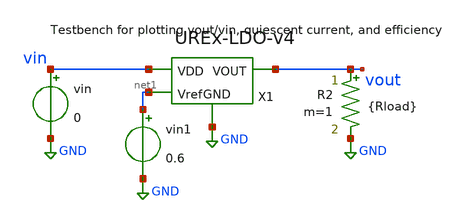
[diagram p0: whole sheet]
** sch_path: xschem/testbenches/VoutvsVin-v4.sch
**.subckt VoutvsVin-v4
vin vin GND 0
R2 vout GND {Rload} m=1
X1 vin vout GND net1 UREx-LDO-v4
vin1 net1 GND 0.6
**** begin user architecture code



.lib /usr/local/share/pdk/sky130A/libs.tech/ngspice/sky130.lib.spice tt
.param Rload = 20
.dc vin 0.5 5 0.1
*.tran 5u 10m

.control
run
let Rload = 20
let iout = vout/Rload
let iq = (-i(vin))-iout
let eff = (iout*vout*100)/((iout+iq)*vin)

plot v(vout)
plot iq
plot eff

.endc


**** end user architecture code
**.ends

* expanding   symbol:  UREx-LDO-v4.sym # of pins=4
** sym_path: xschem/UREx-LDO-v4.sym
** sch_path: xschem/UREx-LDO-v4.sch
.subckt UREx-LDO-v4 VDD VOUT GND Vref
*.ipin VDD
*.opin VOUT
*.ipin GND
*.ipin Vref
XM1 net3 Vref net1 GND sky130_fd_pr__nfet_01v8_lvt L=1 W=0.8 nf=1 ad='int((1 + 1)/2) * 0.8 / 1 * 0.29'
+ as='int((1 + 2)/2) * 0.8 / 1 * 0.29' pd='2*int((1 + 1)/2) * (0.8 / 1 + 0.29)' ps='2*int((1 + 2)/2) * (0.8 / 1 + 0.29)'
+ nrd='0.29 / 0.8 ' nrs='0.29 / 0.8 ' sa=0 sb=0 sd=0 mult=1 m=1
XM2 net2 v+ net1 GND sky130_fd_pr__nfet_01v8_lvt L=1 W=0.8 nf=1 ad='int((1 + 1)/2) * 0.8 / 1 * 0.29'
+ as='int((1 + 2)/2) * 0.8 / 1 * 0.29' pd='2*int((1 + 1)/2) * (0.8 / 1 + 0.29)' ps='2*int((1 + 2)/2) * (0.8 / 1 + 0.29)'
+ nrd='0.29 / 0.8 ' nrs='0.29 / 0.8 ' sa=0 sb=0 sd=0 mult=1 m=1
XM4 net2 net3 VDD VDD sky130_fd_pr__pfet_01v8_lvt L=1 W=0.5 nf=1 ad='int((1 + 1)/2) * 0.5 / 1 * 0.29'
+ as='int((1 + 2)/2) * 0.5 / 1 * 0.29' pd='2*int((1 + 1)/2) * (0.5 / 1 + 0.29)' ps='2*int((1 + 2)/2) * (0.5 / 1 + 0.29)'
+ nrd='0.29 / 0.5 ' nrs='0.29 / 0.5 ' sa=0 sb=0 sd=0 mult=1 m=1
XM3 net3 net3 VDD VDD sky130_fd_pr__pfet_01v8_lvt L=1 W=0.5 nf=1 ad='int((1 + 1)/2) * 0.5 / 1 * 0.29'
+ as='int((1 + 2)/2) * 0.5 / 1 * 0.29' pd='2*int((1 + 1)/2) * (0.5 / 1 + 0.29)' ps='2*int((1 + 2)/2) * (0.5 / 1 + 0.29)'
+ nrd='0.29 / 0.5 ' nrs='0.29 / 0.5 ' sa=0 sb=0 sd=0 mult=1 m=1
XM6 gate net2 VDD VDD sky130_fd_pr__pfet_01v8_lvt L=0.35 W=4.2 nf=1 ad='int((1 + 1)/2) * 4.2 / 1 * 0.29'
+ as='int((1 + 2)/2) * 4.2 / 1 * 0.29' pd='2*int((1 + 1)/2) * (4.2 / 1 + 0.29)' ps='2*int((1 + 2)/2) * (4.2 / 1 + 0.29)'
+ nrd='0.29 / 4.2 ' nrs='0.29 / 4.2 ' sa=0 sb=0 sd=0 mult=1 m=1
XM7 gate net4 GND GND sky130_fd_pr__nfet_01v8_lvt L=0.25 W=5.2 nf=1 ad='int((1 + 1)/2) * 5.2 / 1 * 0.29'
+ as='int((1 + 2)/2) * 5.2 / 1 * 0.29' pd='2*int((1 + 1)/2) * (5.2 / 1 + 0.29)' ps='2*int((1 + 2)/2) * (5.2 / 1 + 0.29)'
+ nrd='0.29 / 5.2 ' nrs='0.29 / 5.2 ' sa=0 sb=0 sd=0 mult=1 m=1
XM9 VOUT gate VDD VDD sky130_fd_pr__pfet_01v8_lvt L=0.35 W=1750 nf=50 ad='int((50 + 1)/2) * 1750 / 50 * 0.29'
+ as='int((50 + 2)/2) * 1750 / 50 * 0.29' pd='2*int((50 + 1)/2) * (1750 / 50 + 0.29)' ps='2*int((50 + 2)/2) * (1750 / 50 + 0.29)'
+ nrd='0.29 / 1750 ' nrs='0.29 / 1750 ' sa=0 sb=0 sd=0 mult=1 m=1
XM10 net4 net5 VDD VDD sky130_fd_pr__pfet_01v8_lvt L=1 W=1 nf=1 ad='int((1 + 1)/2) * 1 / 1 * 0.29' as='int((1 + 2)/2) * 1 / 1 * 0.29'
+ pd='2*int((1 + 1)/2) * (1 / 1 + 0.29)' ps='2*int((1 + 2)/2) * (1 / 1 + 0.29)' nrd='0.29 / 1 ' nrs='0.29 / 1 '
+ sa=0 sb=0 sd=0 mult=1 m=1
XM11 net5 net5 VDD VDD sky130_fd_pr__pfet_01v8_lvt L=1 W=1 nf=1 ad='int((1 + 1)/2) * 1 / 1 * 0.29' as='int((1 + 2)/2) * 1 / 1 * 0.29'
+ pd='2*int((1 + 1)/2) * (1 / 1 + 0.29)' ps='2*int((1 + 2)/2) * (1 / 1 + 0.29)' nrd='0.29 / 1 ' nrs='0.29 / 1 '
+ sa=0 sb=0 sd=0 mult=1 m=1
XM12 net7 net5 VDD VDD sky130_fd_pr__pfet_01v8_lvt L=1 W=1 nf=1 ad='int((1 + 1)/2) * 1 / 1 * 0.29' as='int((1 + 2)/2) * 1 / 1 * 0.29'
+ pd='2*int((1 + 1)/2) * (1 / 1 + 0.29)' ps='2*int((1 + 2)/2) * (1 / 1 + 0.29)' nrd='0.29 / 1 ' nrs='0.29 / 1 '
+ sa=0 sb=0 sd=0 mult=1 m=1
XM13 net7 net7 GND GND sky130_fd_pr__nfet_01v8_lvt L=1 W=2 nf=1 ad='int((1 + 1)/2) * 2 / 1 * 0.29' as='int((1 + 2)/2) * 2 / 1 * 0.29'
+ pd='2*int((1 + 1)/2) * (2 / 1 + 0.29)' ps='2*int((1 + 2)/2) * (2 / 1 + 0.29)' nrd='0.29 / 2 ' nrs='0.29 / 2 '
+ sa=0 sb=0 sd=0 mult=1 m=1
XM14 net5 net7 net6 net6 sky130_fd_pr__nfet_01v8_lvt L=1 W=2.2 nf=1 ad='int((1 + 1)/2) * 2.2 / 1 * 0.29'
+ as='int((1 + 2)/2) * 2.2 / 1 * 0.29' pd='2*int((1 + 1)/2) * (2.2 / 1 + 0.29)' ps='2*int((1 + 2)/2) * (2.2 / 1 + 0.29)'
+ nrd='0.29 / 2.2 ' nrs='0.29 / 2.2 ' sa=0 sb=0 sd=0 mult=1 m=1
XR1 v+ VOUT GND sky130_fd_pr__res_high_po_0p35 L=35.7 mult=1 m=1
XR3 GND v+ GND sky130_fd_pr__res_high_po_0p35 L=53.9 mult=1 m=1
XR2 GND net6 GND sky130_fd_pr__res_high_po_0p35 L=3.1 mult=1 m=1
XC1 gate net2 sky130_fd_pr__cap_mim_m3_1 W=50 L=50 MF=1 m=1
XM5 net1 net4 GND GND sky130_fd_pr__nfet_01v8_lvt L=1 W=1.2 nf=1 ad='int((1 + 1)/2) * 1.2 / 1 * 0.29'
+ as='int((1 + 2)/2) * 1.2 / 1 * 0.29' pd='2*int((1 + 1)/2) * (1.2 / 1 + 0.29)' ps='2*int((1 + 2)/2) * (1.2 / 1 + 0.29)'
+ nrd='0.29 / 1.2 ' nrs='0.29 / 1.2 ' sa=0 sb=0 sd=0 mult=1 m=1
XM8 net4 net4 GND GND sky130_fd_pr__nfet_01v8_lvt L=1 W=1.2 nf=1 ad='int((1 + 1)/2) * 1.2 / 1 * 0.29'
+ as='int((1 + 2)/2) * 1.2 / 1 * 0.29' pd='2*int((1 + 1)/2) * (1.2 / 1 + 0.29)' ps='2*int((1 + 2)/2) * (1.2 / 1 + 0.29)'
+ nrd='0.29 / 1.2 ' nrs='0.29 / 1.2 ' sa=0 sb=0 sd=0 mult=1 m=1
.ends

.GLOBAL GND
.end
